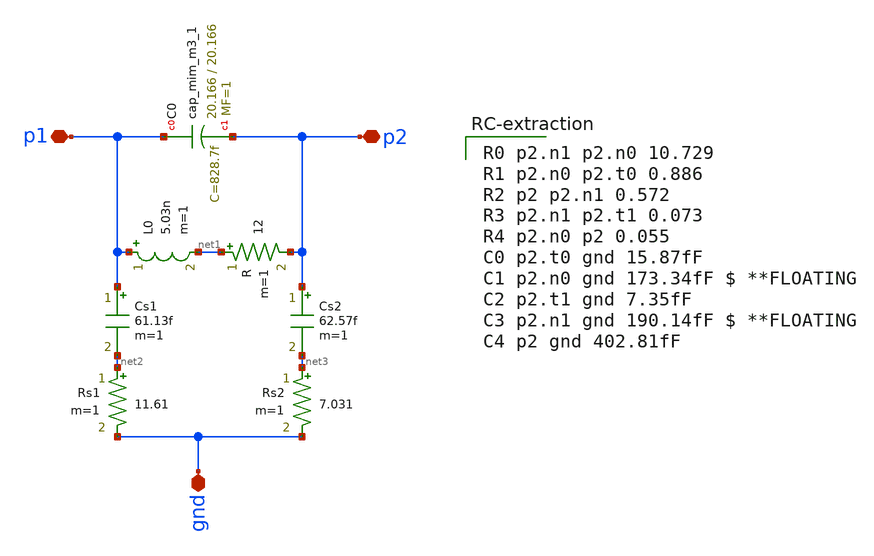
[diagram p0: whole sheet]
** sch_path: xschem/lc_post.sch
**.subckt lc_post p1 p2 gnd
*.iopin p1
*.iopin p2
*.iopin gnd
L0 p1 net1 5.03n m=1
XC0 p1 p2 sky130_fd_pr__cap_mim_m3_1 W=20.166 L=20.166 MF=1 m=1
R net1 p2 12 m=1
Cs2 p2 net3 62.57f m=1
Cs1 p1 net2 61.13f m=1
Rs1 net2 gnd 11.61 m=1
Rs2 net3 gnd 7.031 m=1
**** begin user architecture code

R0 p2.n1 p2.n0 10.729
R1 p2.n0 p2.t0 0.886
R2 p2 p2.n1 0.572
R3 p2.n1 p2.t1 0.073
R4 p2.n0 p2 0.055
C0 p2.t0 gnd 15.87fF
C1 p2.n0 gnd 173.34fF $ **FLOATING
C2 p2.t1 gnd 7.35fF
C3 p2.n1 gnd 190.14fF $ **FLOATING
C4 p2 gnd 402.81fF

**** end user architecture code
**.ends
.end
